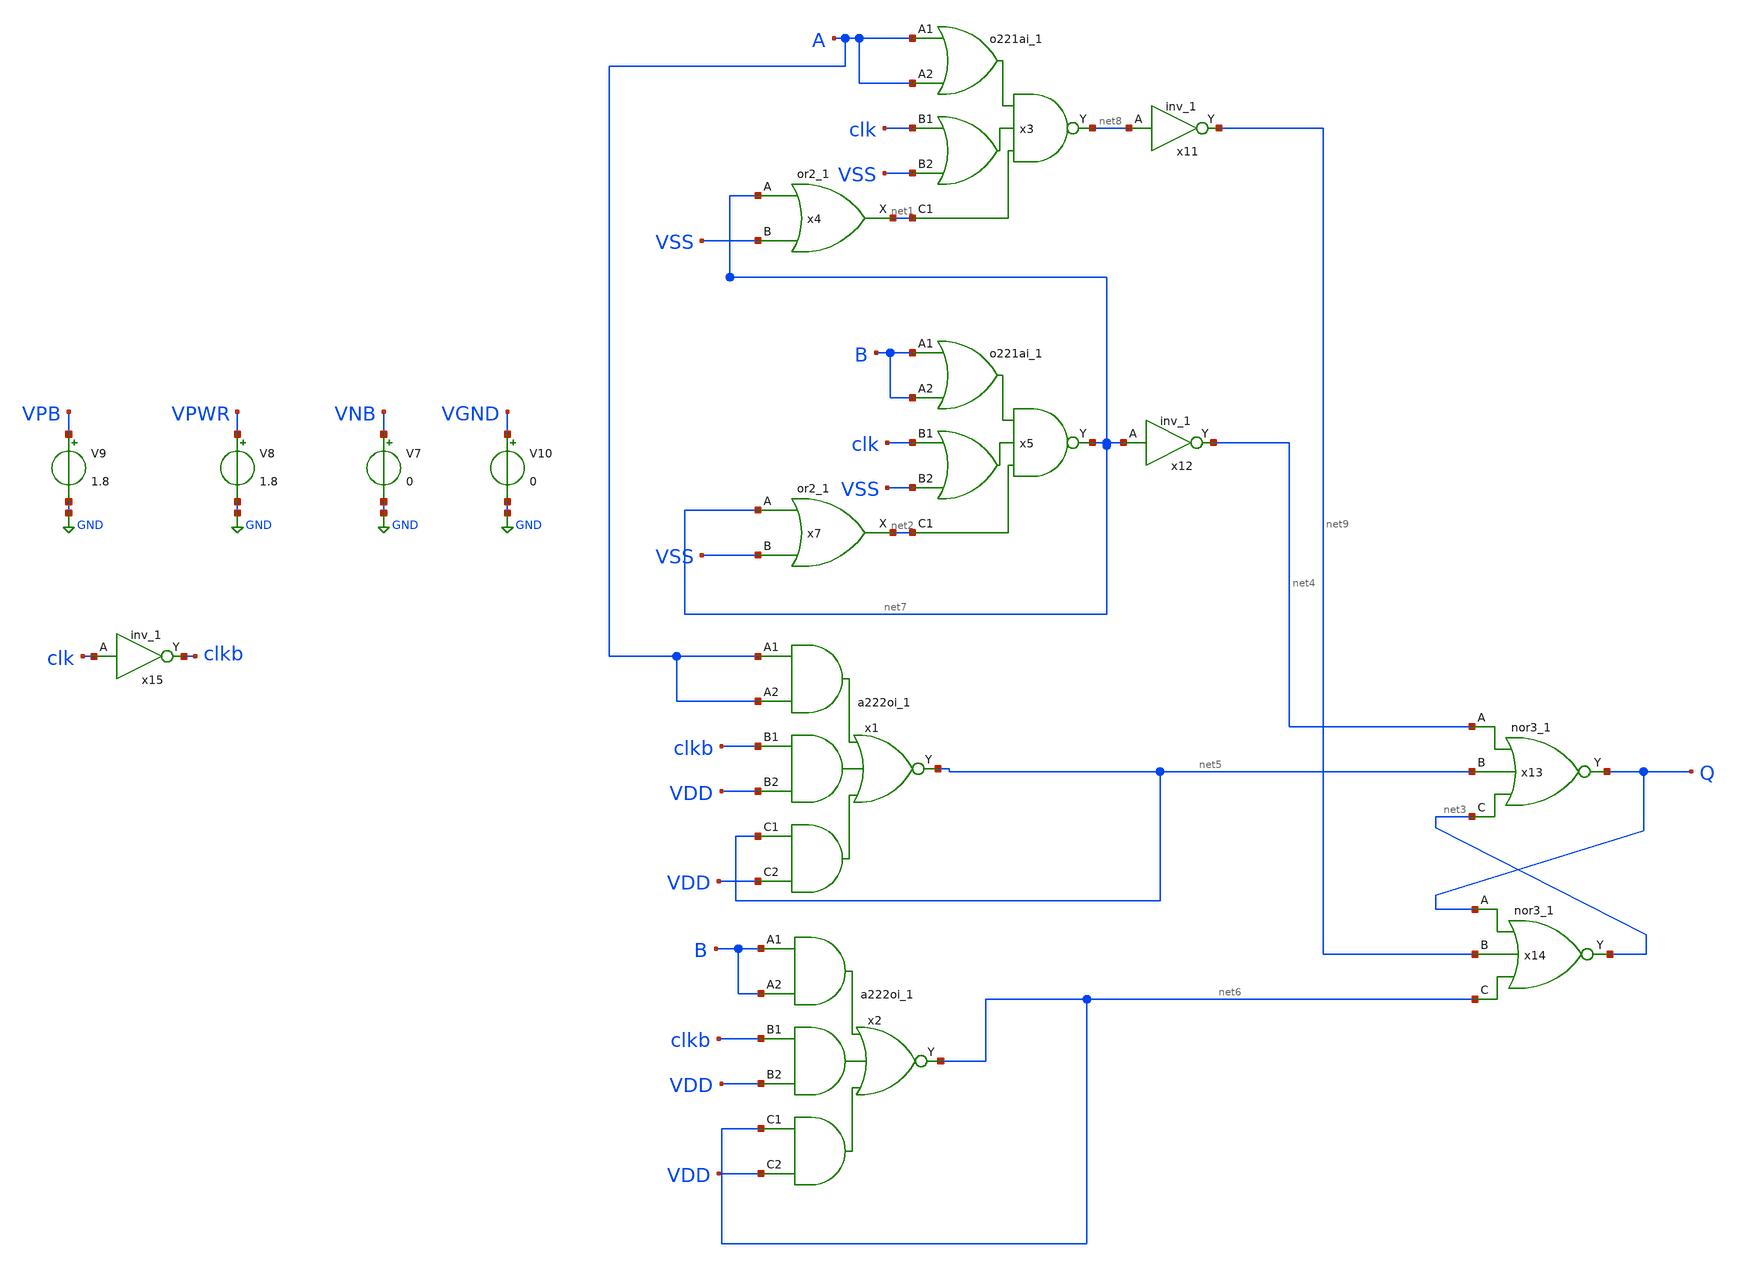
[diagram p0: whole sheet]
** sch_path: cmp/cmpoaisch.sch
**.subckt cmpoaisch
x1 A A clkb VDD net5 VDD VGND VNB VPB VPWR net5 sky130_fd_sc_hd__a222oi_1
x2 B B clkb VDD net6 VDD VGND VNB VPB VPWR net6 sky130_fd_sc_hd__a222oi_1
x4 net7 VSS VGND VNB VPB VPWR net1 sky130_fd_sc_hd__or2_1
x7 net7 VSS VGND VNB VPB VPWR net2 sky130_fd_sc_hd__or2_1
x11 net8 VGND VNB VPB VPWR net9 sky130_fd_sc_hd__inv_1
x12 net7 VGND VNB VPB VPWR net4 sky130_fd_sc_hd__inv_1
x13 net4 net5 net3 VGND VNB VPB VPWR Q sky130_fd_sc_hd__nor3_1
x14 Q net9 net6 VGND VNB VPB VPWR net3 sky130_fd_sc_hd__nor3_1
V7 VNB GND 0
V8 VPWR GND 1.8
V9 VPB GND 1.8
V10 VGND GND 0
x15 clk VGND VNB VPB VPWR clkb sky130_fd_sc_hd__inv_1
x3 A A clk VSS net1 VGND VNB VPB VPWR net8 sky130_fd_sc_hd__o221ai_1
x5 B B clk VSS net2 VGND VNB VPB VPWR net7 sky130_fd_sc_hd__o221ai_1
**.ends
.GLOBAL GND
.end
